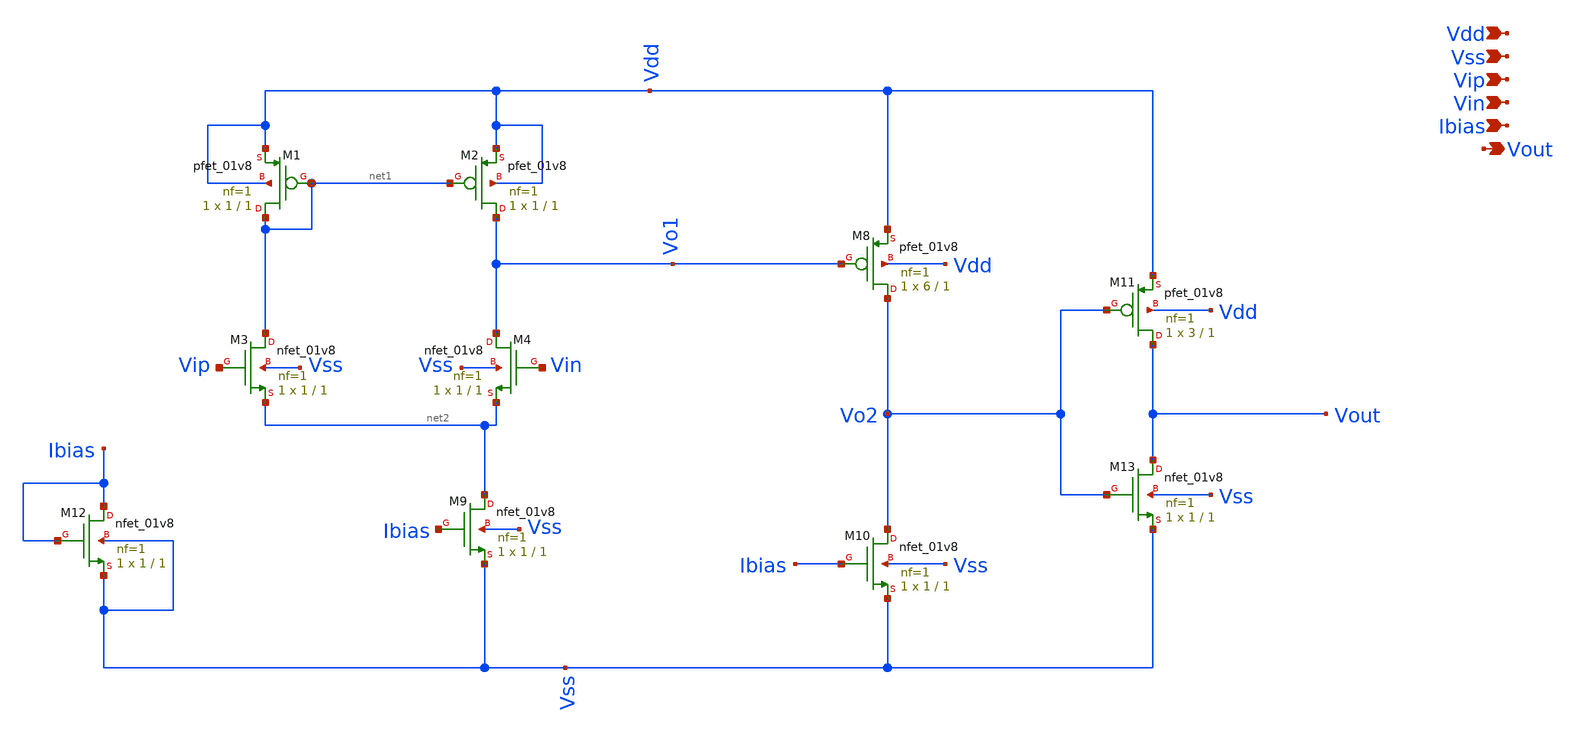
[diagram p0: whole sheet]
** sch_path: temp_sensor_sky130nm/design/TEMP_SENSOR_SKY130NM/COMPARATOR.sch
**.subckt COMPARATOR Vdd Vss Vip Vin Ibias Vout
*.ipin Vdd
*.ipin Vss
*.ipin Vip
*.ipin Vin
*.ipin Ibias
*.opin Vout
XM1 net1 net1 Vdd Vdd sky130_fd_pr__pfet_01v8 L=1 W=1 nf=1 ad='int((nf+1)/2) * W/nf * 0.29' as='int((nf+2)/2) * W/nf * 0.29'
+ pd='2*int((nf+1)/2) * (W/nf + 0.29)' ps='2*int((nf+2)/2) * (W/nf + 0.29)' nrd='0.29 / W' nrs='0.29 / W'
+ sa=0 sb=0 sd=0 mult=1 m=1
XM2 Vo1 net1 Vdd Vdd sky130_fd_pr__pfet_01v8 L=1 W=1 nf=1 ad='int((nf+1)/2) * W/nf * 0.29' as='int((nf+2)/2) * W/nf * 0.29'
+ pd='2*int((nf+1)/2) * (W/nf + 0.29)' ps='2*int((nf+2)/2) * (W/nf + 0.29)' nrd='0.29 / W' nrs='0.29 / W'
+ sa=0 sb=0 sd=0 mult=1 m=1
XM3 net1 Vip net2 Vss sky130_fd_pr__nfet_01v8 L=1 W=1 nf=1 ad='int((nf+1)/2) * W/nf * 0.29' as='int((nf+2)/2) * W/nf * 0.29'
+ pd='2*int((nf+1)/2) * (W/nf + 0.29)' ps='2*int((nf+2)/2) * (W/nf + 0.29)' nrd='0.29 / W' nrs='0.29 / W'
+ sa=0 sb=0 sd=0 mult=1 m=1
XM4 Vo1 Vin net2 Vss sky130_fd_pr__nfet_01v8 L=1 W=1 nf=1 ad='int((nf+1)/2) * W/nf * 0.29' as='int((nf+2)/2) * W/nf * 0.29'
+ pd='2*int((nf+1)/2) * (W/nf + 0.29)' ps='2*int((nf+2)/2) * (W/nf + 0.29)' nrd='0.29 / W' nrs='0.29 / W'
+ sa=0 sb=0 sd=0 mult=1 m=1
XM9 net2 Ibias Vss Vss sky130_fd_pr__nfet_01v8 L=1 W=1 nf=1 ad='int((nf+1)/2) * W/nf * 0.29' as='int((nf+2)/2) * W/nf * 0.29'
+ pd='2*int((nf+1)/2) * (W/nf + 0.29)' ps='2*int((nf+2)/2) * (W/nf + 0.29)' nrd='0.29 / W' nrs='0.29 / W'
+ sa=0 sb=0 sd=0 mult=1 m=1
XM8 Vo2 Vo1 Vdd Vdd sky130_fd_pr__pfet_01v8 L=1 W=6 nf=1 ad='int((nf+1)/2) * W/nf * 0.29' as='int((nf+2)/2) * W/nf * 0.29'
+ pd='2*int((nf+1)/2) * (W/nf + 0.29)' ps='2*int((nf+2)/2) * (W/nf + 0.29)' nrd='0.29 / W' nrs='0.29 / W'
+ sa=0 sb=0 sd=0 mult=1 m=1
XM10 Vo2 Ibias Vss Vss sky130_fd_pr__nfet_01v8 L=1 W=1 nf=1 ad='int((nf+1)/2) * W/nf * 0.29' as='int((nf+2)/2) * W/nf * 0.29'
+ pd='2*int((nf+1)/2) * (W/nf + 0.29)' ps='2*int((nf+2)/2) * (W/nf + 0.29)' nrd='0.29 / W' nrs='0.29 / W'
+ sa=0 sb=0 sd=0 mult=1 m=1
XM11 Vout Vo2 Vdd Vdd sky130_fd_pr__pfet_01v8 L=1 W=3 nf=1 ad='int((nf+1)/2) * W/nf * 0.29' as='int((nf+2)/2) * W/nf * 0.29'
+ pd='2*int((nf+1)/2) * (W/nf + 0.29)' ps='2*int((nf+2)/2) * (W/nf + 0.29)' nrd='0.29 / W' nrs='0.29 / W'
+ sa=0 sb=0 sd=0 mult=1 m=1
XM13 Vout Vo2 Vss Vss sky130_fd_pr__nfet_01v8 L=1 W=1 nf=1 ad='int((nf+1)/2) * W/nf * 0.29' as='int((nf+2)/2) * W/nf * 0.29'
+ pd='2*int((nf+1)/2) * (W/nf + 0.29)' ps='2*int((nf+2)/2) * (W/nf + 0.29)' nrd='0.29 / W' nrs='0.29 / W'
+ sa=0 sb=0 sd=0 mult=1 m=1
XM12 Ibias Ibias Vss Vss sky130_fd_pr__nfet_01v8 L=1 W=1 nf=1 ad='int((nf+1)/2) * W/nf * 0.29' as='int((nf+2)/2) * W/nf * 0.29'
+ pd='2*int((nf+1)/2) * (W/nf + 0.29)' ps='2*int((nf+2)/2) * (W/nf + 0.29)' nrd='0.29 / W' nrs='0.29 / W'
+ sa=0 sb=0 sd=0 mult=1 m=1
**.ends
.end
